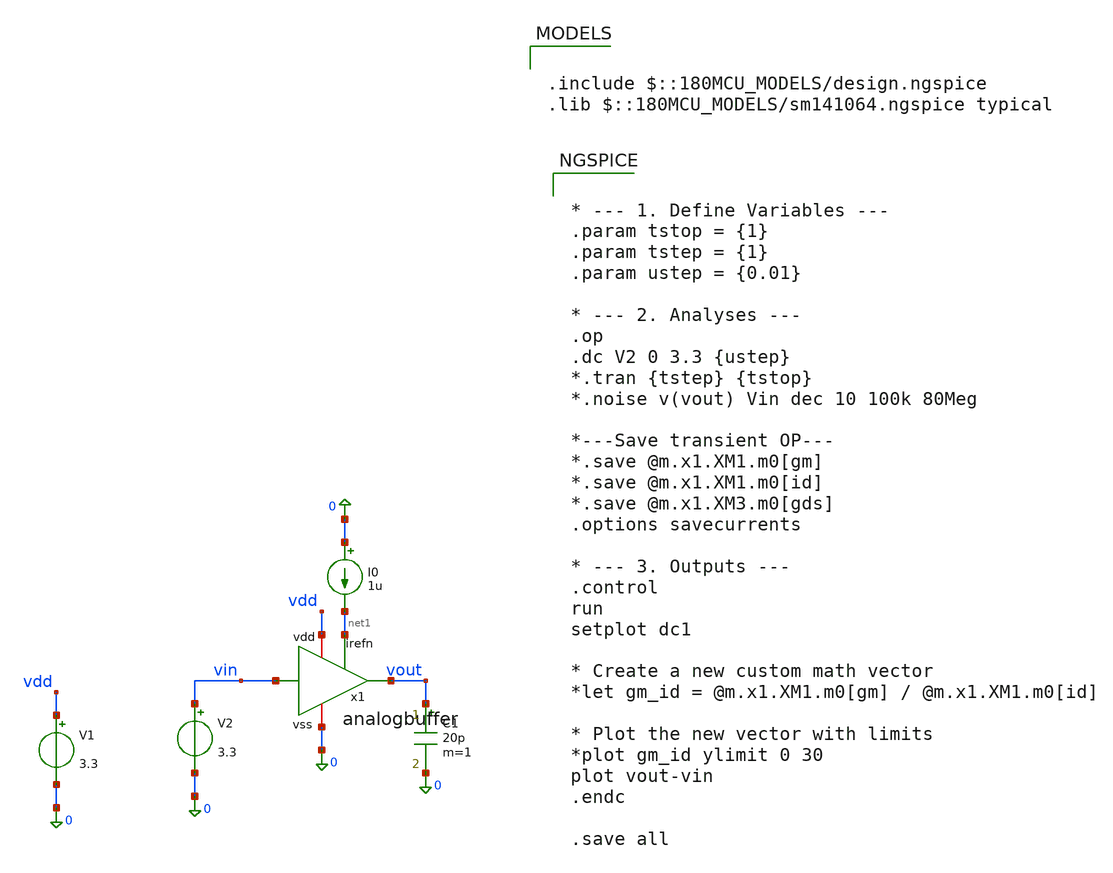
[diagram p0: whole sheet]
** sch_path: Tobias/2026 07 14 Intermediate Results/analogbuffer/analogbuffer-tb.sch
**.subckt analogbuffer-tb
x1 vdd net1 vin vout 0 analogbuffer
I0 0 net1 1u
V1 vdd 0 3.3
V2 vin 0 3.3
C1 vout 0 20p m=1
**** begin user architecture code


* --- 1. Define Variables ---
.param tstop = {1}
.param tstep = {1}
.param ustep = {0.01}

* --- 2. Analyses ---
.op
.dc V2 0 3.3 {ustep}
*.tran {tstep} {tstop}
*.noise v(vout) Vin dec 10 100k 80Meg

*---Save transient OP---
*.save @m.x1.XM1.m0[gm]
*.save @m.x1.XM1.m0[id]
*.save @m.x1.XM3.m0[gds]
.options savecurrents

* --- 3. Outputs ---
.control
run
setplot dc1

* Create a new custom math vector
*let gm_id = @m.x1.XM1.m0[gm] / @m.x1.XM1.m0[id]

* Plot the new vector with limits
*plot gm_id ylimit 0 30
plot vout-vin
.endc

.save all



.include $::180MCU_MODELS/design.ngspice
.lib $::180MCU_MODELS/sm141064.ngspice typical

**** end user architecture code
**.ends
.end
